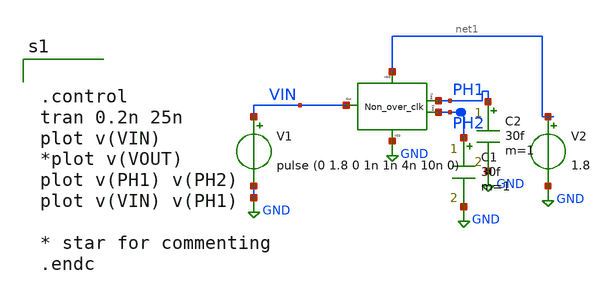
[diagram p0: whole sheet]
** sch_path: xschem/xschem_BGR_Top/Sigma_Delta/Non_over_clk/Non_over_clk_TB.sch
**.subckt Non_over_clk_TB
V1 VIN GND pulse (0 1.8 0 1n 1n 4n 10n 0)
V2 net1 GND 1.8
X1 PH2 net1 GND PH1 VIN Non_over_clk
C1 PH2 GND 30f m=1
C2 PH1 GND 30f m=1
**** begin user architecture code


.control
tran 0.2n 25n
plot v(VIN)
*plot v(VOUT)
plot v(PH1) v(PH2)
plot v(VIN) v(PH1)

* star for commenting
.endc


** opencircuitdesign pdks install
.lib $::SKYWATER_MODELS/sky130.lib.spice tt


**** end user architecture code
**.ends

* expanding   symbol:  Sigma_Delta/Non_over_clk/Non_over_clk.sym # of pins=5
** sym_path: xschem/xschem_BGR_Top/Sigma_Delta/Non_over_clk/Non_over_clk.sym
** sch_path: xschem/xschem_BGR_Top/Sigma_Delta/Non_over_clk/Non_over_clk.sch
.subckt Non_over_clk PH2 VDD VSS PH1 CLK
*.iopin VDD
*.iopin VSS
*.iopin CLK
*.iopin PH1
*.iopin PH2
X1 VSS VDD CLK net1 Inverter
X2 VSS VDD net9 PH1 Inverter
X3 VSS VDD net8 PH2 Inverter
X4 VSS VDD net3 net2 INV_1x64
X5 VSS VDD net5 net4 INV_1x64
XNOR1 VDD VSS net1 PH2 net3 NOR
XNOR2 VDD VSS CLK PH1 net5 NOR
X8 VSS VDD net6 net8 Inverter
X9 VSS VDD net7 net9 Inverter
X6 VSS VDD net2 net7 INV_1x64
X7 VSS VDD net4 net6 INV_1x64
.ends


* expanding   symbol:  Sigma_Delta/Inverter/Inverter.sym # of pins=4
** sym_path: xschem/xschem_BGR_Top/Sigma_Delta/Inverter/Inverter.sym
** sch_path: xschem/xschem_BGR_Top/Sigma_Delta/Inverter/Inverter.sch
.subckt Inverter VSS VDD VIN VOUT
*.ipin VIN
*.iopin VDD
*.iopin VSS
*.opin VOUT
XM1 VOUT VIN VSS VSS sky130_fd_pr__nfet_01v8 L=0.15 W=0.9 nf=1 ad='int((nf+1)/2) * W/nf * 0.29' as='int((nf+2)/2) * W/nf * 0.29'
+ pd='2*int((nf+1)/2) * (W/nf + 0.29)' ps='2*int((nf+2)/2) * (W/nf + 0.29)' nrd='0.29 / W' nrs='0.29 / W'
+ sa=0 sb=0 sd=0 mult=1 m=1
XM2 VOUT VIN VDD VDD sky130_fd_pr__pfet_01v8 L=0.15 W=0.9 nf=2 ad='int((nf+1)/2) * W/nf * 0.29' as='int((nf+2)/2) * W/nf * 0.29'
+ pd='2*int((nf+1)/2) * (W/nf + 0.29)' ps='2*int((nf+2)/2) * (W/nf + 0.29)' nrd='0.29 / W' nrs='0.29 / W'
+ sa=0 sb=0 sd=0 mult=1 m=1
.ends


* expanding   symbol:  Sigma_Delta/INV_1x64/INV_1x64.sym # of pins=4
** sym_path: xschem/xschem_BGR_Top/Sigma_Delta/INV_1x64/INV_1x64.sym
** sch_path: xschem/xschem_BGR_Top/Sigma_Delta/INV_1x64/INV_1x64.sch
.subckt INV_1x64 VSS VDD VIN VOUT
*.ipin VIN
*.iopin VDD
*.iopin VSS
*.opin VOUT
XM1 VOUT VIN net1 VSS sky130_fd_pr__nfet_01v8 L=0.15 W=0.425 nf=1 ad='int((nf+1)/2) * W/nf * 0.29' as='int((nf+2)/2) * W/nf * 0.29'
+ pd='2*int((nf+1)/2) * (W/nf + 0.29)' ps='2*int((nf+2)/2) * (W/nf + 0.29)' nrd='0.29 / W' nrs='0.29 / W'
+ sa=0 sb=0 sd=0 mult=1 m=1
XM2 VOUT VIN net2 VDD sky130_fd_pr__pfet_01v8 L=0.15 W=0.425 nf=1 ad='int((nf+1)/2) * W/nf * 0.29' as='int((nf+2)/2) * W/nf * 0.29'
+ pd='2*int((nf+1)/2) * (W/nf + 0.29)' ps='2*int((nf+2)/2) * (W/nf + 0.29)' nrd='0.29 / W' nrs='0.29 / W'
+ sa=0 sb=0 sd=0 mult=1 m=1
XM3 net2 VIN net3 VDD sky130_fd_pr__pfet_01v8 L=0.15 W=0.425 nf=1 ad='int((nf+1)/2) * W/nf * 0.29' as='int((nf+2)/2) * W/nf * 0.29'
+ pd='2*int((nf+1)/2) * (W/nf + 0.29)' ps='2*int((nf+2)/2) * (W/nf + 0.29)' nrd='0.29 / W' nrs='0.29 / W'
+ sa=0 sb=0 sd=0 mult=1 m=1
XM4 net3 VIN net4 VDD sky130_fd_pr__pfet_01v8 L=0.15 W=0.425 nf=1 ad='int((nf+1)/2) * W/nf * 0.29' as='int((nf+2)/2) * W/nf * 0.29'
+ pd='2*int((nf+1)/2) * (W/nf + 0.29)' ps='2*int((nf+2)/2) * (W/nf + 0.29)' nrd='0.29 / W' nrs='0.29 / W'
+ sa=0 sb=0 sd=0 mult=1 m=1
XM5 net4 VIN net8 VDD sky130_fd_pr__pfet_01v8 L=0.15 W=0.425 nf=1 ad='int((nf+1)/2) * W/nf * 0.29' as='int((nf+2)/2) * W/nf * 0.29'
+ pd='2*int((nf+1)/2) * (W/nf + 0.29)' ps='2*int((nf+2)/2) * (W/nf + 0.29)' nrd='0.29 / W' nrs='0.29 / W'
+ sa=0 sb=0 sd=0 mult=1 m=1
XM6 net1 VIN net5 VSS sky130_fd_pr__nfet_01v8 L=0.15 W=0.425 nf=1 ad='int((nf+1)/2) * W/nf * 0.29' as='int((nf+2)/2) * W/nf * 0.29'
+ pd='2*int((nf+1)/2) * (W/nf + 0.29)' ps='2*int((nf+2)/2) * (W/nf + 0.29)' nrd='0.29 / W' nrs='0.29 / W'
+ sa=0 sb=0 sd=0 mult=1 m=1
XM7 net5 VIN net6 VSS sky130_fd_pr__nfet_01v8 L=0.15 W=0.425 nf=1 ad='int((nf+1)/2) * W/nf * 0.29' as='int((nf+2)/2) * W/nf * 0.29'
+ pd='2*int((nf+1)/2) * (W/nf + 0.29)' ps='2*int((nf+2)/2) * (W/nf + 0.29)' nrd='0.29 / W' nrs='0.29 / W'
+ sa=0 sb=0 sd=0 mult=1 m=1
XM8 net6 VIN net7 VSS sky130_fd_pr__nfet_01v8 L=0.15 W=0.425 nf=1 ad='int((nf+1)/2) * W/nf * 0.29' as='int((nf+2)/2) * W/nf * 0.29'
+ pd='2*int((nf+1)/2) * (W/nf + 0.29)' ps='2*int((nf+2)/2) * (W/nf + 0.29)' nrd='0.29 / W' nrs='0.29 / W'
+ sa=0 sb=0 sd=0 mult=1 m=1
XM9 net7 VIN VSS VSS sky130_fd_pr__nfet_01v8 L=0.15 W=0.425 nf=1 ad='int((nf+1)/2) * W/nf * 0.29' as='int((nf+2)/2) * W/nf * 0.29'
+ pd='2*int((nf+1)/2) * (W/nf + 0.29)' ps='2*int((nf+2)/2) * (W/nf + 0.29)' nrd='0.29 / W' nrs='0.29 / W'
+ sa=0 sb=0 sd=0 mult=1 m=1
XM10 net8 VIN VDD VDD sky130_fd_pr__pfet_01v8 L=0.15 W=0.425 nf=1 ad='int((nf+1)/2) * W/nf * 0.29' as='int((nf+2)/2) * W/nf * 0.29'
+ pd='2*int((nf+1)/2) * (W/nf + 0.29)' ps='2*int((nf+2)/2) * (W/nf + 0.29)' nrd='0.29 / W' nrs='0.29 / W'
+ sa=0 sb=0 sd=0 mult=1 m=1
.ends


* expanding   symbol:  Sigma_Delta/Nor/NOR.sym # of pins=5
** sym_path: xschem/xschem_BGR_Top/Sigma_Delta/Nor/NOR.sym
** sch_path: xschem/xschem_BGR_Top/Sigma_Delta/Nor/NOR.sch
.subckt NOR VDD VSS A B OUT
*.iopin VDD
*.iopin VSS
*.iopin A
*.iopin B
*.iopin OUT
XM2 OUT A VSS VSS sky130_fd_pr__nfet_01v8 L=0.15 W=0.5 nf=1 ad='int((nf+1)/2) * W/nf * 0.29' as='int((nf+2)/2) * W/nf * 0.29'
+ pd='2*int((nf+1)/2) * (W/nf + 0.29)' ps='2*int((nf+2)/2) * (W/nf + 0.29)' nrd='0.29 / W' nrs='0.29 / W'
+ sa=0 sb=0 sd=0 mult=1 m=1
XM3 net1 A VDD VDD sky130_fd_pr__pfet_01v8 L=0.15 W=0.5 nf=1 ad='int((nf+1)/2) * W/nf * 0.29' as='int((nf+2)/2) * W/nf * 0.29'
+ pd='2*int((nf+1)/2) * (W/nf + 0.29)' ps='2*int((nf+2)/2) * (W/nf + 0.29)' nrd='0.29 / W' nrs='0.29 / W'
+ sa=0 sb=0 sd=0 mult=1 m=1
XM1 OUT B net1 VDD sky130_fd_pr__pfet_01v8 L=0.15 W=0.5 nf=1 ad='int((nf+1)/2) * W/nf * 0.29' as='int((nf+2)/2) * W/nf * 0.29'
+ pd='2*int((nf+1)/2) * (W/nf + 0.29)' ps='2*int((nf+2)/2) * (W/nf + 0.29)' nrd='0.29 / W' nrs='0.29 / W'
+ sa=0 sb=0 sd=0 mult=1 m=1
XM4 OUT B VSS VSS sky130_fd_pr__nfet_01v8 L=0.15 W=0.5 nf=1 ad='int((nf+1)/2) * W/nf * 0.29' as='int((nf+2)/2) * W/nf * 0.29'
+ pd='2*int((nf+1)/2) * (W/nf + 0.29)' ps='2*int((nf+2)/2) * (W/nf + 0.29)' nrd='0.29 / W' nrs='0.29 / W'
+ sa=0 sb=0 sd=0 mult=1 m=1
.ends

.GLOBAL GND
.end
